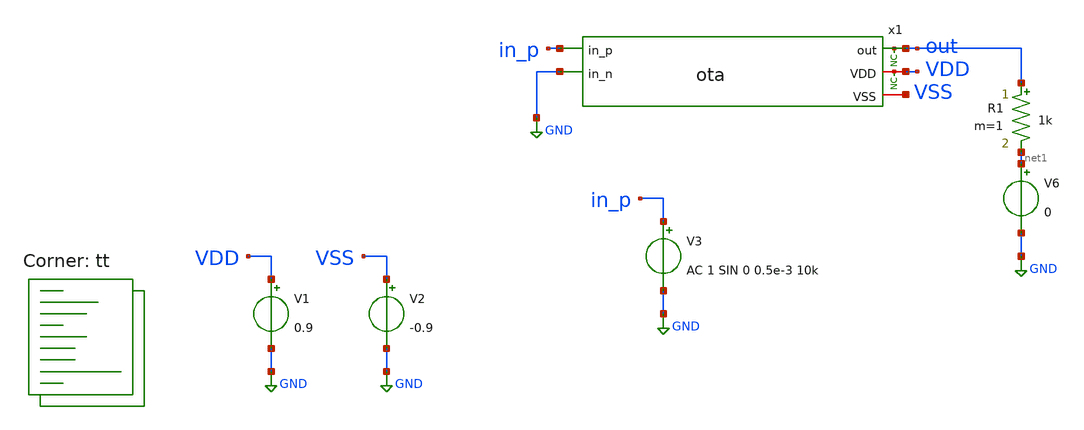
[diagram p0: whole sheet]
** sch_path: xschem/tests/ota/ota_ac_gm_test.sch
**.subckt ota_ac_gm_test
V1 VDD GND 0.9
V2 VSS GND -0.9
V3 in_p GND AC 1 SIN 0 0.5e-3 10k
* noconn VDD
* noconn out
V6 net1 GND 0
R1 out net1 1k m=1
x1 out in_p GND VDD VSS ota
**** begin user architecture code
.lib $::SKYWATER_MODELS/sky130.lib.spice tt
 *.lib $::SKYWATER_MODELS/sky130.lib.spice tt
.include $::SKYWATER_STDCELLS/sky130_fd_sc_hd.spice




* ngspice commands
* ngspice commands
.options list act
.options method=gear
.temp 25

.control
save all
ac dec 10 1k 10G
plot out in_p
plot i(v6)
plot -i(v6)/in_p

meas tran outptp pp v(out) from=0s to=300us
meas tran outmean avg v(out) from=0s to=300us

let gain = 20*log10($&outptp/0.002)
echo gain = $&gain

write ota2_test.raw
.endc



**** end user architecture code
**.ends

* expanding   symbol:  src/ota/ota.sym # of pins=5
** sym_path: xschem/src/ota/ota.sym
** sch_path: xschem/src/ota/ota.sch
.subckt ota out in_p in_n VDD VSS
*.iopin VDD
*.ipin in_p
*.opin out
*.iopin VSS
*.ipin in_n
XM1 net3 VDD VSS VSS sky130_fd_pr__nfet_01v8 L=0.15 W=1.5 nf=1 ad='int((nf+1)/2) * W/nf * 0.29' as='int((nf+2)/2) * W/nf * 0.29'
+ pd='2*int((nf+1)/2) * (W/nf + 0.29)' ps='2*int((nf+2)/2) * (W/nf + 0.29)' nrd='0.29 / W' nrs='0.29 / W'
+ sa=0 sb=0 sd=0 mult=1 m=1
XM2 net1 net1 VDD VDD sky130_fd_pr__pfet_01v8 L=0.15 W=20 nf=1 ad='int((nf+1)/2) * W/nf * 0.29' as='int((nf+2)/2) * W/nf * 0.29'
+ pd='2*int((nf+1)/2) * (W/nf + 0.29)' ps='2*int((nf+2)/2) * (W/nf + 0.29)' nrd='0.29 / W' nrs='0.29 / W'
+ sa=0 sb=0 sd=0 mult=1 m=1
XM3 net2 net1 VDD VDD sky130_fd_pr__pfet_01v8 L=0.15 W=20 nf=1 ad='int((nf+1)/2) * W/nf * 0.29' as='int((nf+2)/2) * W/nf * 0.29'
+ pd='2*int((nf+1)/2) * (W/nf + 0.29)' ps='2*int((nf+2)/2) * (W/nf + 0.29)' nrd='0.29 / W' nrs='0.29 / W'
+ sa=0 sb=0 sd=0 mult=1 m=1
XM6 VSS VDD VDD VSS sky130_fd_pr__nfet_01v8 L=0.15 W=1 nf=1 ad='int((nf+1)/2) * W/nf * 0.29' as='int((nf+2)/2) * W/nf * 0.29'
+ pd='2*int((nf+1)/2) * (W/nf + 0.29)' ps='2*int((nf+2)/2) * (W/nf + 0.29)' nrd='0.29 / W' nrs='0.29 / W'
+ sa=0 sb=0 sd=0 mult=1 m=1
XM7 net1 in_p net3 VSS sky130_fd_pr__nfet_01v8_lvt L=0.15 W=10 nf=1 ad='int((nf+1)/2) * W/nf * 0.29'
+ as='int((nf+2)/2) * W/nf * 0.29' pd='2*int((nf+1)/2) * (W/nf + 0.29)' ps='2*int((nf+2)/2) * (W/nf + 0.29)'
+ nrd='0.29 / W' nrs='0.29 / W' sa=0 sb=0 sd=0 mult=1 m=1
XM4 net3 in_n net2 VSS sky130_fd_pr__nfet_01v8_lvt L=0.15 W=10 nf=1 ad='int((nf+1)/2) * W/nf * 0.29'
+ as='int((nf+2)/2) * W/nf * 0.29' pd='2*int((nf+1)/2) * (W/nf + 0.29)' ps='2*int((nf+2)/2) * (W/nf + 0.29)'
+ nrd='0.29 / W' nrs='0.29 / W' sa=0 sb=0 sd=0 mult=1 m=1
XM8 out VDD VSS VSS sky130_fd_pr__nfet_01v8 L=0.365 W=1 nf=1 ad='int((nf+1)/2) * W/nf * 0.29' as='int((nf+2)/2) * W/nf * 0.29'
+ pd='2*int((nf+1)/2) * (W/nf + 0.29)' ps='2*int((nf+2)/2) * (W/nf + 0.29)' nrd='0.29 / W' nrs='0.29 / W'
+ sa=0 sb=0 sd=0 mult=1 m=1
XM5 out net2 VDD VDD sky130_fd_pr__pfet_01v8 L=0.15 W=30 nf=1 ad='int((nf+1)/2) * W/nf * 0.29' as='int((nf+2)/2) * W/nf * 0.29'
+ pd='2*int((nf+1)/2) * (W/nf + 0.29)' ps='2*int((nf+2)/2) * (W/nf + 0.29)' nrd='0.29 / W' nrs='0.29 / W'
+ sa=0 sb=0 sd=0 mult=1 m=1
XC1 net2 out sky130_fd_pr__cap_mim_m3_1 W=2 L=2 MF=1 m=1
.ends

.GLOBAL GND
.end
